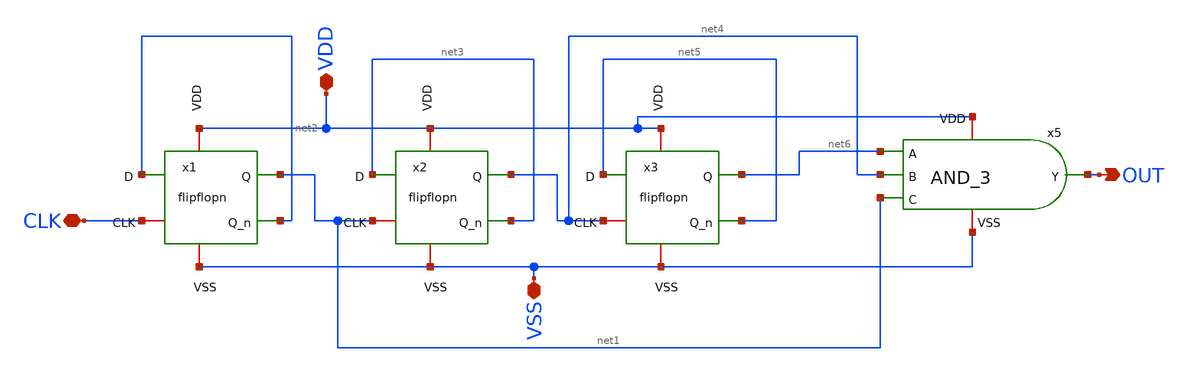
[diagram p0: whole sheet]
** sch_path: XSCHEM/cont.sch
**.subckt cont OUT CLK VDD VSS
*.opin OUT
*.iopin CLK
*.iopin VDD
*.iopin VSS
x1 CLK net2 VDD net1 net2 VSS flipflopn
x2 net1 net3 VDD net4 net3 VSS flipflopn
x3 net4 net5 VDD net6 net5 VSS flipflopn
x5 VDD net6 net4 net1 OUT VSS AND_3
**.ends

* expanding   symbol:  flipflopn.sym # of pins=6
** sym_path: flipflopn.sym
** sch_path: flipflopn.sch
.subckt flipflopn CLK Q_n VDD Q D VSS
*.ipin D
*.opin Q
*.iopin CLK
*.iopin VDD
*.iopin VSS
*.opin Q_n
XMN0 net1 net7 net2 VSS sg13_lv_nmos w=740.00n l=130.00n ng=1 m=1 mm_ok=1
XMP0 net1 CLK net2 VDD sg13_lv_pmos w=1.12u l=130.00n ng=1 m=1 mm_ok=1
XMN1 net2 CLK net3 VSS sg13_lv_nmos w=740.00n l=130.00n ng=1 m=1 mm_ok=1
XMP1 net2 net7 net3 VDD sg13_lv_pmos w=1.12u l=130.00n ng=1 m=1 mm_ok=1
XMN2 net4 CLK net5 VSS sg13_lv_nmos w=740.00n l=130.00n ng=1 m=1 mm_ok=1
XMP2 net4 net7 net5 VDD sg13_lv_pmos w=1.12u l=130.00n ng=1 m=1 mm_ok=1
XMN3 net5 net7 net6 VSS sg13_lv_nmos w=740.00n l=130.00n ng=1 m=1 mm_ok=1
XMP3 net5 CLK net6 VDD sg13_lv_pmos w=1.12u l=130.00n ng=1 m=1 mm_ok=1
x8 VDD net1 D VSS my_inv
x1 VDD net4 net2 VSS my_inv
x2 VDD net7 CLK VSS my_inv
x3 VDD net3 net4 VSS my_inv
x4 VDD Q_n net5 VSS my_inv
x5 VDD Q Q_n VSS my_inv
x6 VDD net6 Q_n VSS my_inv
.ends


* expanding   symbol:  AND_3.sym # of pins=6
** sym_path: XSCHEM/AND_3.sym
** sch_path: XSCHEM/AND_3.sch
.subckt AND_3 VDD A B C Y VSS
*.ipin A
*.iopin VDD
*.iopin VSS
*.ipin B
*.ipin C
*.opin Y
XMN0 net2 B net3 VSS sg13_lv_nmos w=740.00n l=130.00n ng=1 m=1 mm_ok=1
XMP0 net1 A VDD VDD sg13_lv_pmos w=1.12u l=130.00n ng=1 m=1 mm_ok=1
XMN1 net1 A net2 VSS sg13_lv_nmos w=740.00n l=130.00n ng=1 m=1 mm_ok=1
XMN2 net3 C VSS VSS sg13_lv_nmos w=740.00n l=130.00n ng=1 m=1 mm_ok=1
XMP1 net1 B VDD VDD sg13_lv_pmos w=1.12u l=130.00n ng=1 m=1 mm_ok=1
XMP2 net1 C VDD VDD sg13_lv_pmos w=1.12u l=130.00n ng=1 m=1 mm_ok=1
XMN3 Y net1 VSS VSS sg13_lv_nmos w=740.00n l=130.00n ng=1 m=1 mm_ok=1
XMP3 Y net1 VDD VDD sg13_lv_pmos w=1.12u l=130.00n ng=1 m=1 mm_ok=1
.ends


* expanding   symbol:  my_inv.sym # of pins=4
** sym_path: xschem/my_inv.sym
** sch_path: xschem/my_inv.sch
.subckt my_inv VDD Y A VSS
*.opin Y
*.ipin A
*.iopin VDD
*.iopin VSS
XMN0 Y A VSS VSS sg13_lv_nmos w=740.00n l=130.00n ng=1 m=1 mm_ok=1
XMP0 Y A VDD VDD sg13_lv_pmos w=1.12u l=130.00n ng=1 m=1 mm_ok=1
.ends

.end
